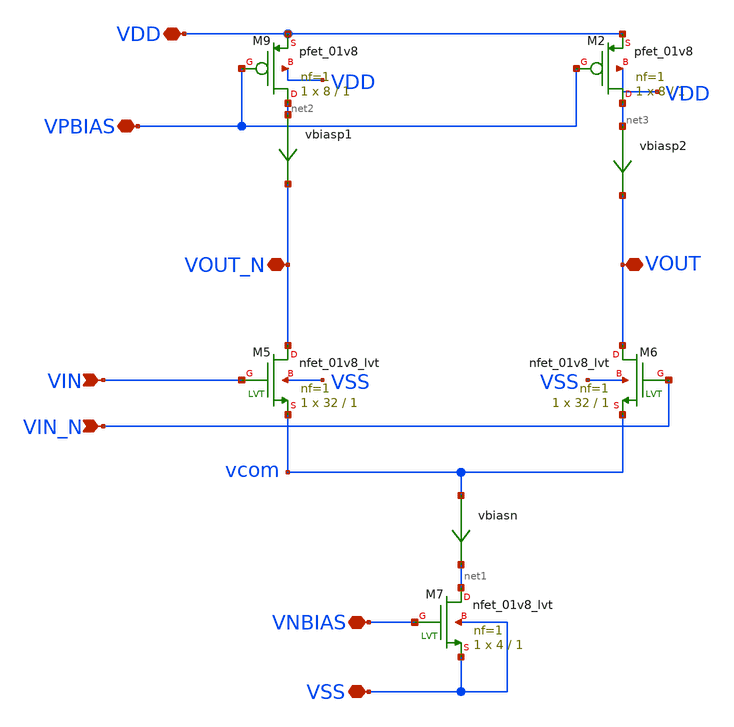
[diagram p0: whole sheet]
** sch_path: tt_um_emilian_rf_playground/xschem/opamp1.sch
**.subckt opamp1 VIN VIN_N VOUT VOUT_N VPBIAS VNBIAS VDD VSS
*.ipin VIN
*.ipin VIN_N
*.iopin VOUT
*.iopin VOUT_N
*.iopin VPBIAS
*.iopin VNBIAS
*.iopin VDD
*.iopin VSS
XM5 VOUT_N VIN vcom VSS sky130_fd_pr__nfet_01v8_lvt L=1 W=32 nf=1 ad='int((nf+1)/2) * W/nf * 0.29' as='int((nf+2)/2) * W/nf * 0.29'
+ pd='2*int((nf+1)/2) * (W/nf + 0.29)' ps='2*int((nf+2)/2) * (W/nf + 0.29)' nrd='0.29 / W' nrs='0.29 / W'
+ sa=0 sb=0 sd=0 mult=1 m=1
vbiasp1 net2 VOUT_N 0
.save i(vbiasp1)
XM2 net3 VPBIAS VDD VDD sky130_fd_pr__pfet_01v8 L=1 W=8 nf=1 ad='int((nf+1)/2) * W/nf * 0.29' as='int((nf+2)/2) * W/nf * 0.29'
+ pd='2*int((nf+1)/2) * (W/nf + 0.29)' ps='2*int((nf+2)/2) * (W/nf + 0.29)' nrd='0.29 / W' nrs='0.29 / W'
+ sa=0 sb=0 sd=0 mult=1 m=1
vbiasp2 net3 VOUT 0
.save i(vbiasp2)
vbiasn vcom net1 0
.save i(vbiasn)
XM7 net1 VNBIAS VSS VSS sky130_fd_pr__nfet_01v8_lvt L=1 W=4 nf=1 ad='int((nf+1)/2) * W/nf * 0.29' as='int((nf+2)/2) * W/nf * 0.29'
+ pd='2*int((nf+1)/2) * (W/nf + 0.29)' ps='2*int((nf+2)/2) * (W/nf + 0.29)' nrd='0.29 / W' nrs='0.29 / W'
+ sa=0 sb=0 sd=0 mult=1 m=1
XM6 VOUT VIN_N vcom VSS sky130_fd_pr__nfet_01v8_lvt L=1 W=32 nf=1 ad='int((nf+1)/2) * W/nf * 0.29' as='int((nf+2)/2) * W/nf * 0.29'
+ pd='2*int((nf+1)/2) * (W/nf + 0.29)' ps='2*int((nf+2)/2) * (W/nf + 0.29)' nrd='0.29 / W' nrs='0.29 / W'
+ sa=0 sb=0 sd=0 mult=1 m=1
XM9 net2 VPBIAS VDD VDD sky130_fd_pr__pfet_01v8 L=1 W=8 nf=1 ad='int((nf+1)/2) * W/nf * 0.29' as='int((nf+2)/2) * W/nf * 0.29'
+ pd='2*int((nf+1)/2) * (W/nf + 0.29)' ps='2*int((nf+2)/2) * (W/nf + 0.29)' nrd='0.29 / W' nrs='0.29 / W'
+ sa=0 sb=0 sd=0 mult=1 m=1
**.ends
.end
